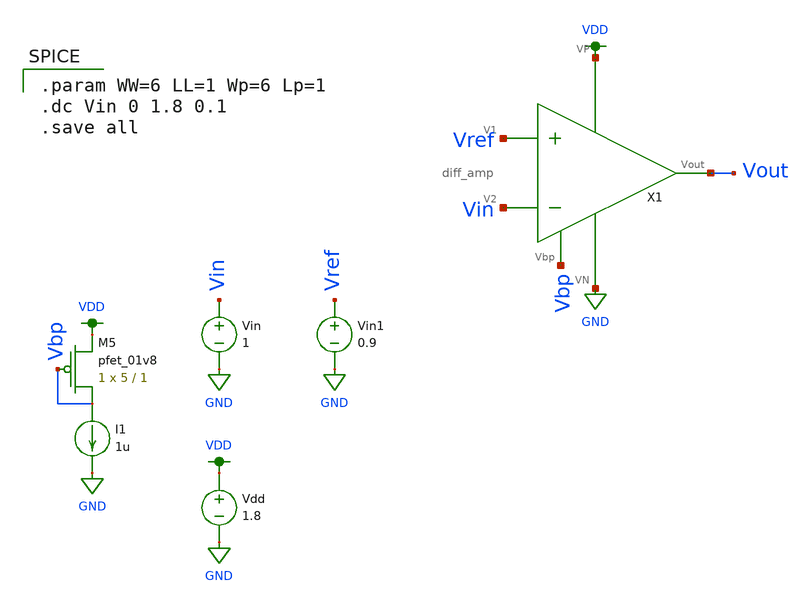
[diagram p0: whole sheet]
** sch_path: schematic/comparator.sch
**.subckt comparator
Vdd VDD GND 1.8
XM5 Vbp Vbp VDD VDD sky130_fd_pr__pfet_01v8 L=1 W=5 nf=1 ad='int((nf+1)/2) * W/nf * 0.29' as='int((nf+2)/2) * W/nf * 0.29'
+ pd='2*int((nf+1)/2) * (W/nf + 0.29)' ps='2*int((nf+2)/2) * (W/nf + 0.29)' nrd='0.29 / W' nrs='0.29 / W'
+ sa=0 sb=0 sd=0 mult=1 m=1
I1 Vbp GND 1u
Vin Vin GND 1
X1 VDD Vbp Vout Vref Vin GND diff_amp
Vin1 Vref GND 0.9
**** begin user architecture code

.param WW=6 LL=1 Wp=6 Lp=1
.dc Vin 0 1.8 0.1
.save all


.option wnflag=1
.param MC_SWITCH=0.0
.lib ~/skywater/skywater-pdk/libraries/sky130_fd_pr_ngspice/latest/models/sky130.lib.spice tt

**** end user architecture code
**.ends
.GLOBAL GND
.GLOBAL VDD
.end
